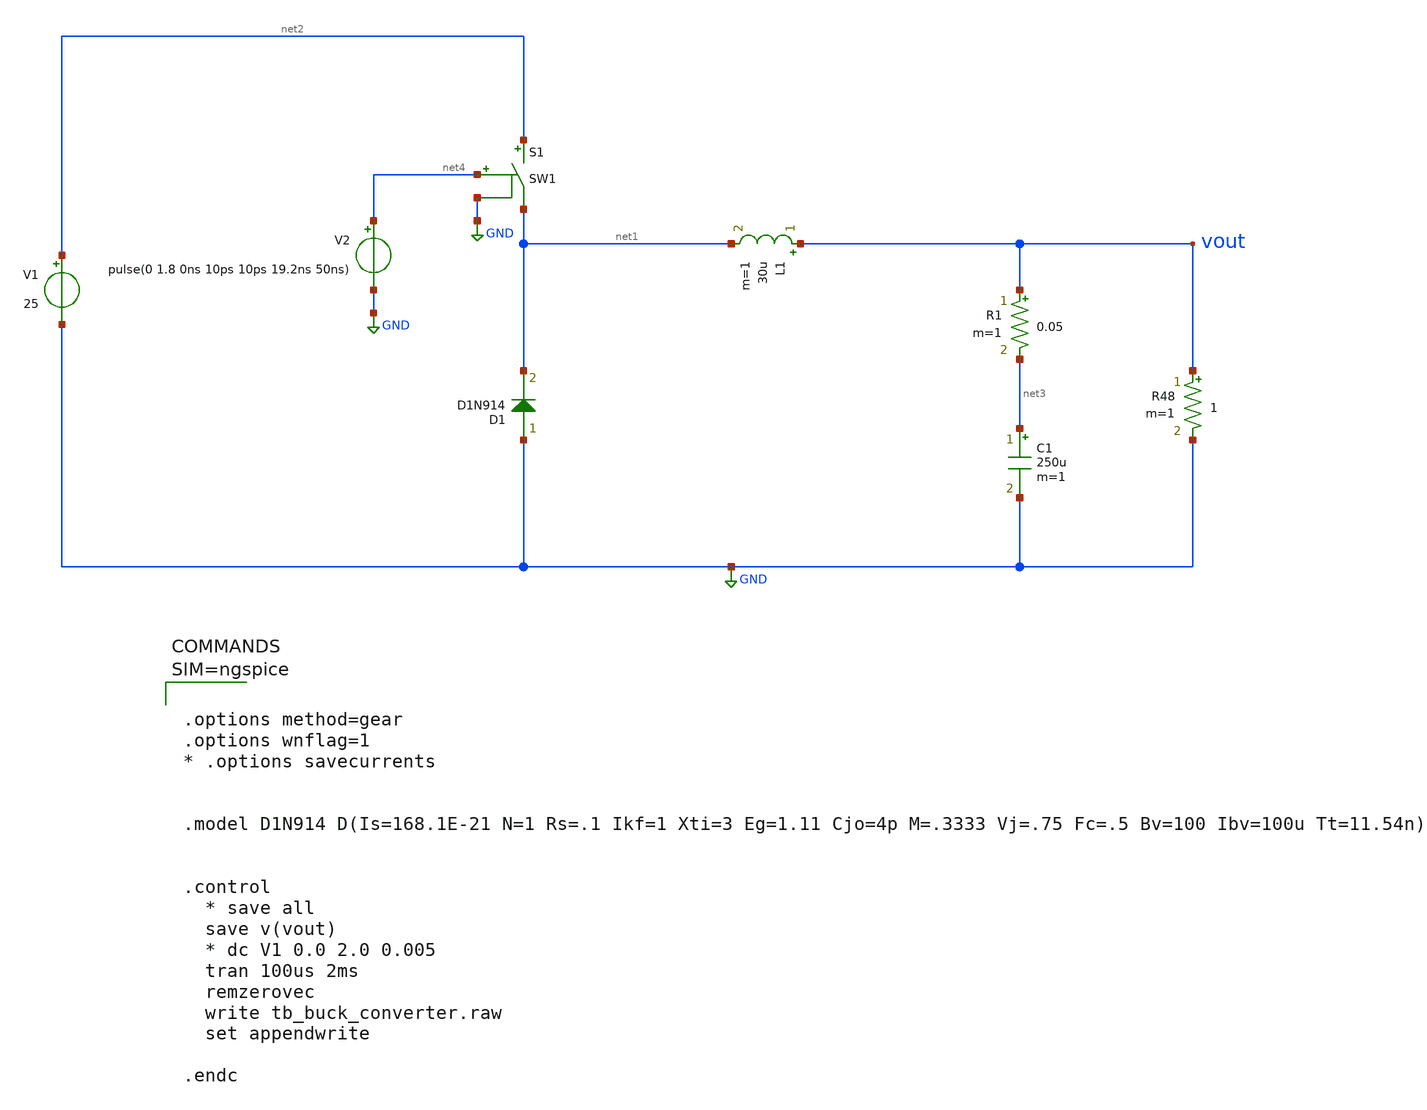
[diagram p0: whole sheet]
** sch_path: projects/ASU/EEE572/schematic/tb_buck_converter.sch
**.subckt tb_buck_converter
V1 net2 GND 25
R48 vout GND 1 m=1
D1 GND net1 D1N914 area=1
L1 vout net1 30u m=1
C1 net3 GND 250u m=1
R1 vout net3 0.05 m=1
V2 net4 GND pulse(0 1.8 0ns 10ps 10ps 19.2ns 50ns)
S1 net2 net1 net4 GND SW1
**** begin user architecture code



.options method=gear
.options wnflag=1
* .options savecurrents


.model D1N914 D(Is=168.1E-21 N=1 Rs=.1 Ikf=1 Xti=3 Eg=1.11 Cjo=4p M=.3333 Vj=.75 Fc=.5 Bv=100
+ Ibv=100u Tt=11.54n)


.control
  * save all
  save v(vout)
  * dc V1 0.0 2.0 0.005
  tran 100us 2ms
  remzerovec
  write tb_buck_converter.raw
  set appendwrite

.endc





**** end user architecture code
**.ends
.GLOBAL GND
**** begin user architecture code
.MODEL SW1 SW( VT=0.9 VH=0.01 RON=0.01 ROFF=10G )
**** end user architecture code
.end
